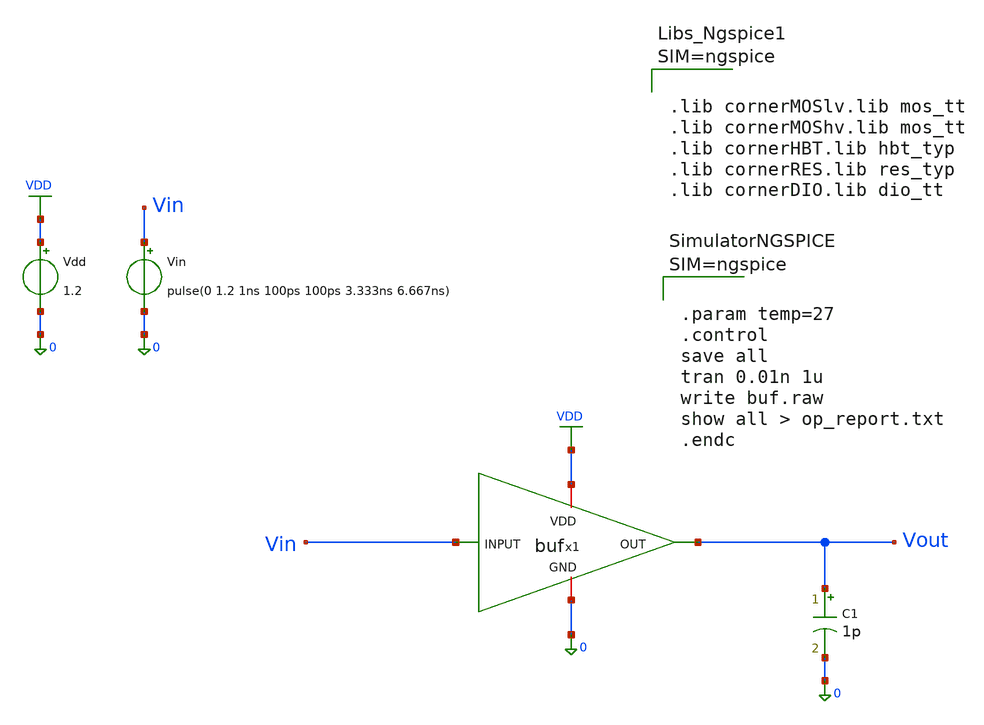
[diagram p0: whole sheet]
** sch_path: schematics/buf/buf_sym.sch
**.subckt buf_sym
x1 VDD Vin Vout 0 buf
Vdd VDD 0 1.2
Vin Vin 0 pulse(0 1.2 1ns 100ps 100ps 3.333ns 6.667ns)
C1 Vout 0 1p m=1
**** begin user architecture code



.lib cornerMOSlv.lib mos_tt
.lib cornerMOShv.lib mos_tt
.lib cornerHBT.lib hbt_typ
.lib cornerRES.lib res_typ
.lib cornerDIO.lib dio_tt






.param temp=27
.control
save all
tran 0.01n 1u
write buf.raw
show all > op_report.txt
.endc



**** end user architecture code
**.ends

* expanding   symbol:  buf.sym # of pins=4
** sym_path: schematics/buf/buf.sym
** sch_path: schematics/buf/buf.sch
.subckt buf VDD INPUT OUT GND
*.ipin INPUT
*.iopin VDD
*.iopin GND
*.opin OUT
XM9 OUT net3 VDD VDD sg13_hv_pmos w=10u l=0.4u ng=1 m=4 mm_ok=1
XM6 net3 net2 VDD VDD sg13_hv_pmos w=10u l=0.4u ng=1 m=2 mm_ok=1
XM4 net2 net1 VDD VDD sg13_hv_pmos w=10u l=0.4u ng=1 m=1 mm_ok=1
XM2 net1 INPUT VDD VDD sg13_hv_pmos w=5u l=0.4u ng=1 m=1 mm_ok=1
XM1 OUT net3 GND GND sg13_hv_nmos w=10u l=0.45u ng=1 m=4 mm_ok=1
XM3 net3 net2 GND GND sg13_hv_nmos w=10u l=0.45u ng=1 m=2 mm_ok=1
XM5 net2 net1 GND GND sg13_hv_nmos w=10u l=0.45u ng=1 m=1 mm_ok=1
XM7 net1 INPUT GND GND sg13_hv_nmos w=5u l=0.45u ng=1 m=1 mm_ok=1
.ends

.GLOBAL VDD
.end
